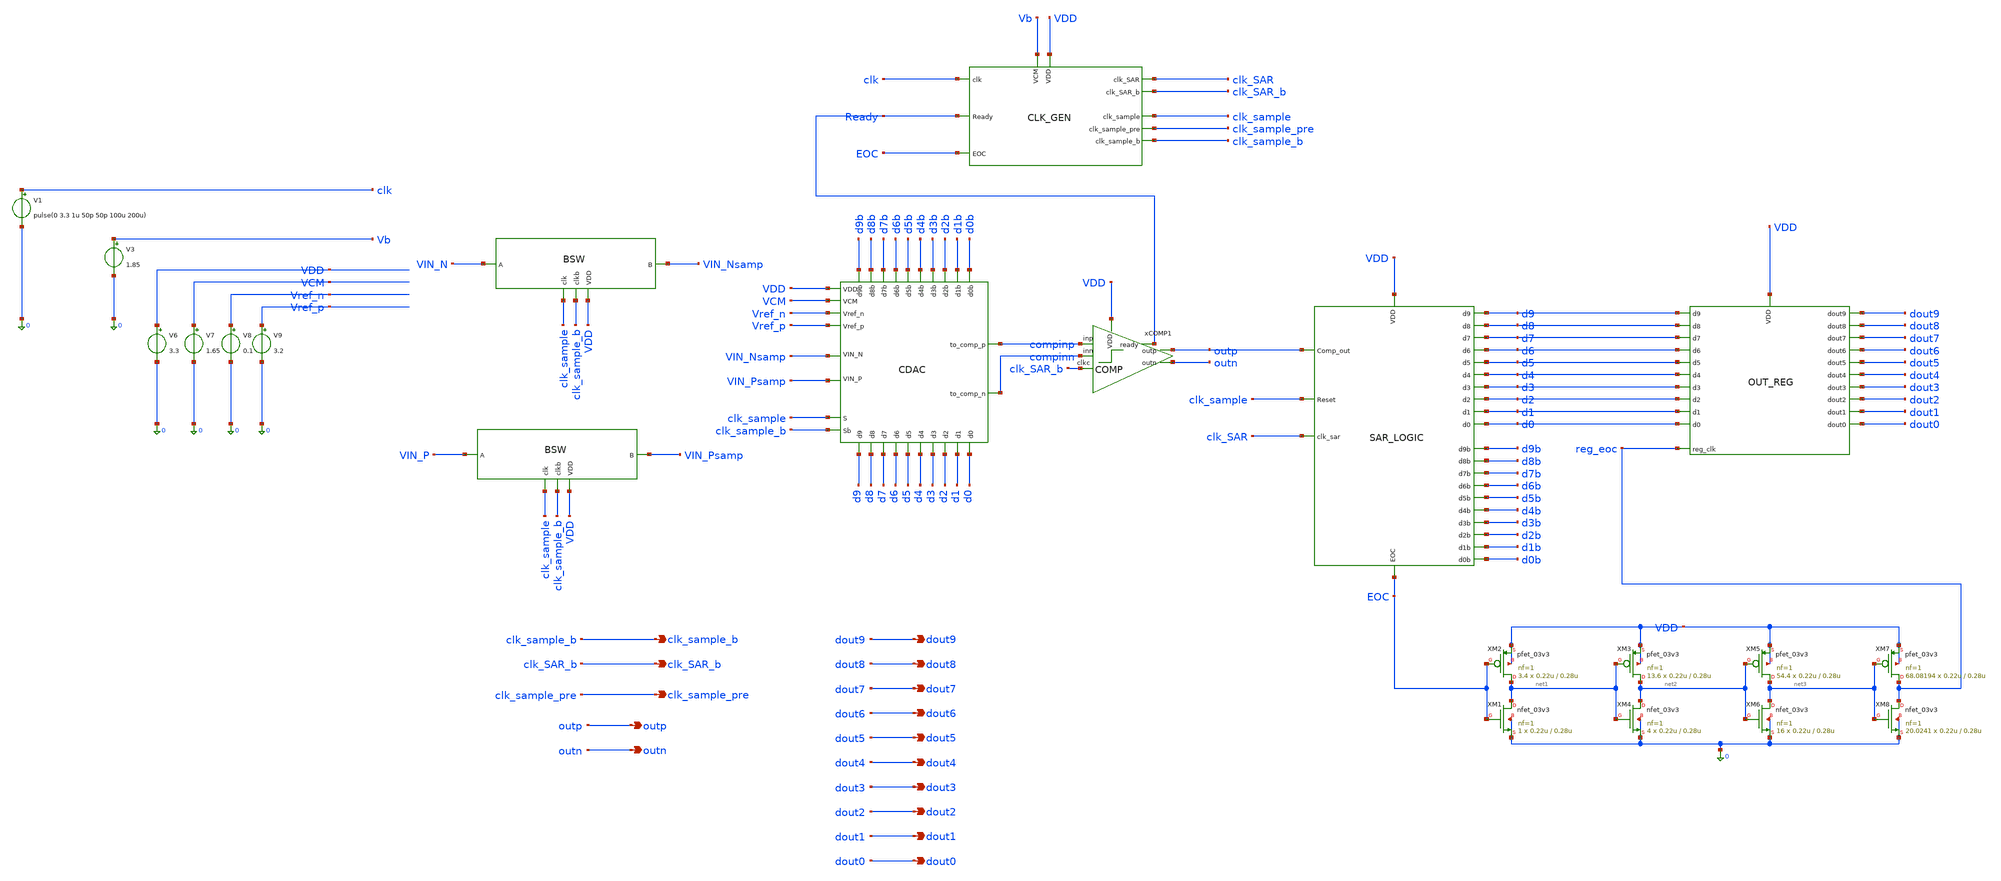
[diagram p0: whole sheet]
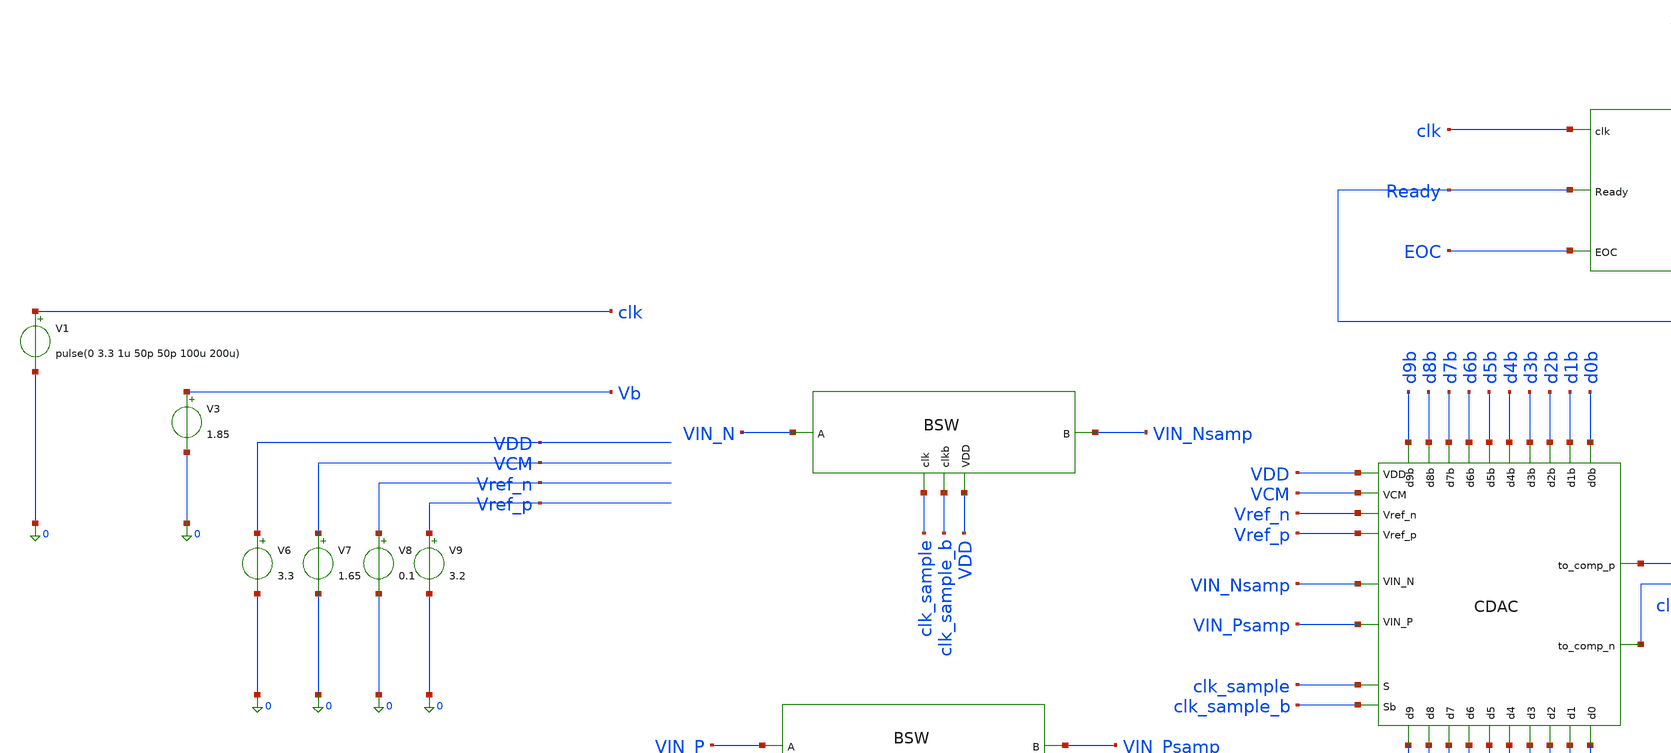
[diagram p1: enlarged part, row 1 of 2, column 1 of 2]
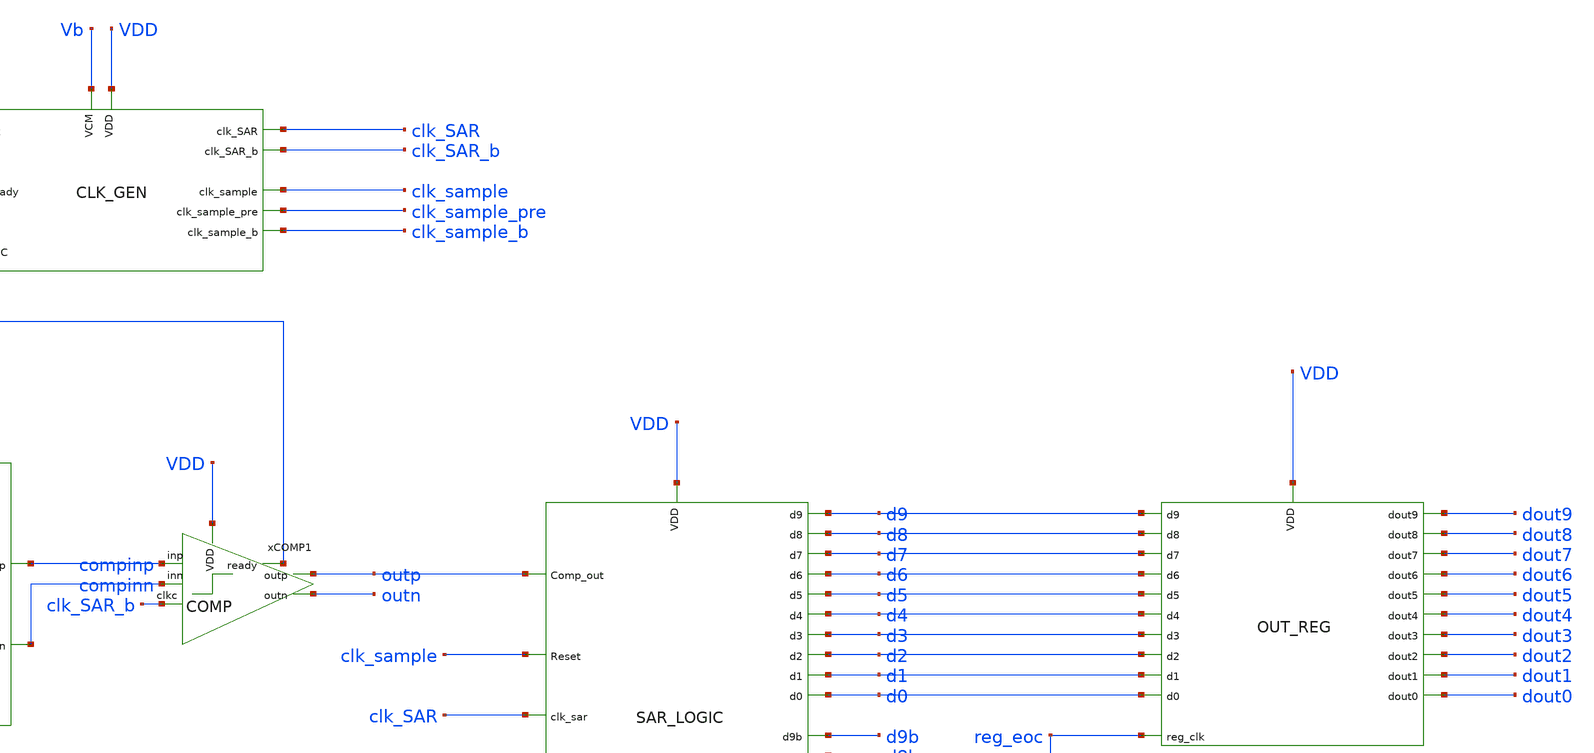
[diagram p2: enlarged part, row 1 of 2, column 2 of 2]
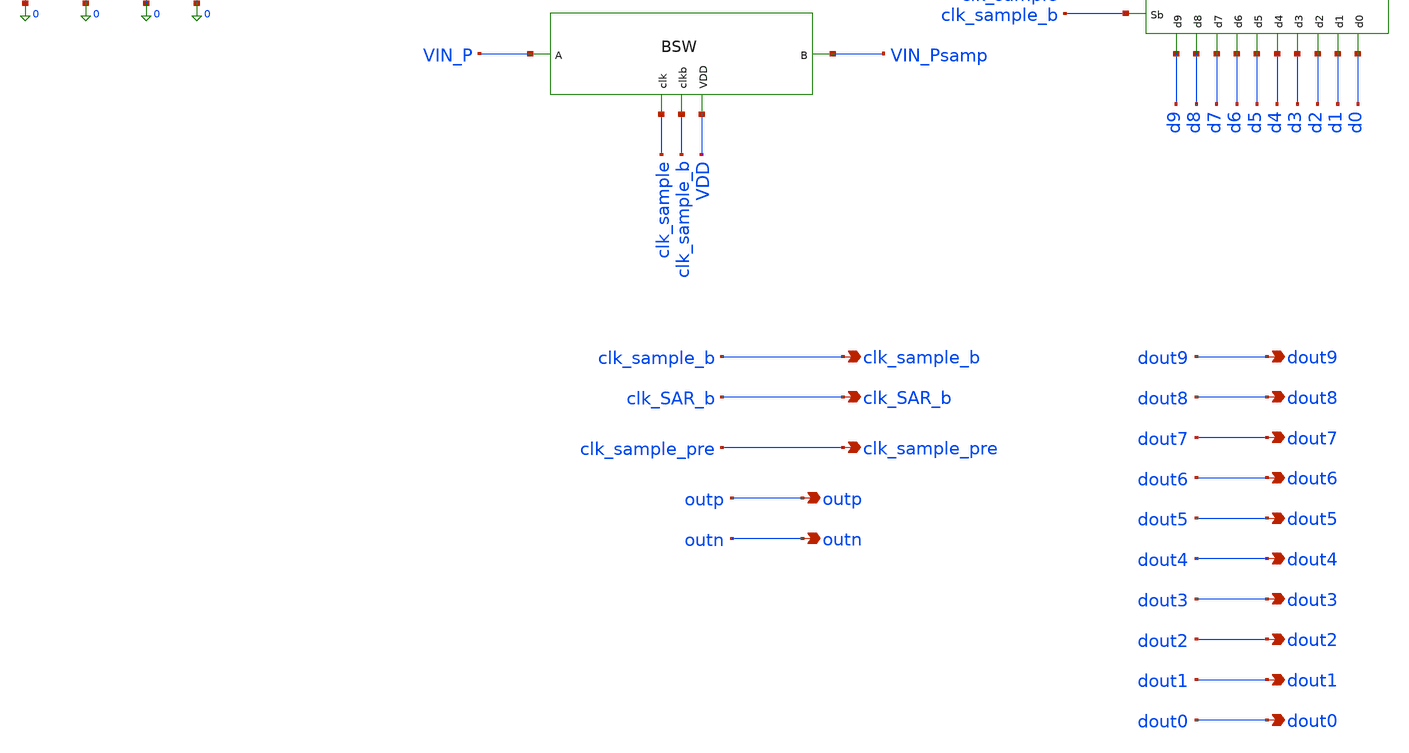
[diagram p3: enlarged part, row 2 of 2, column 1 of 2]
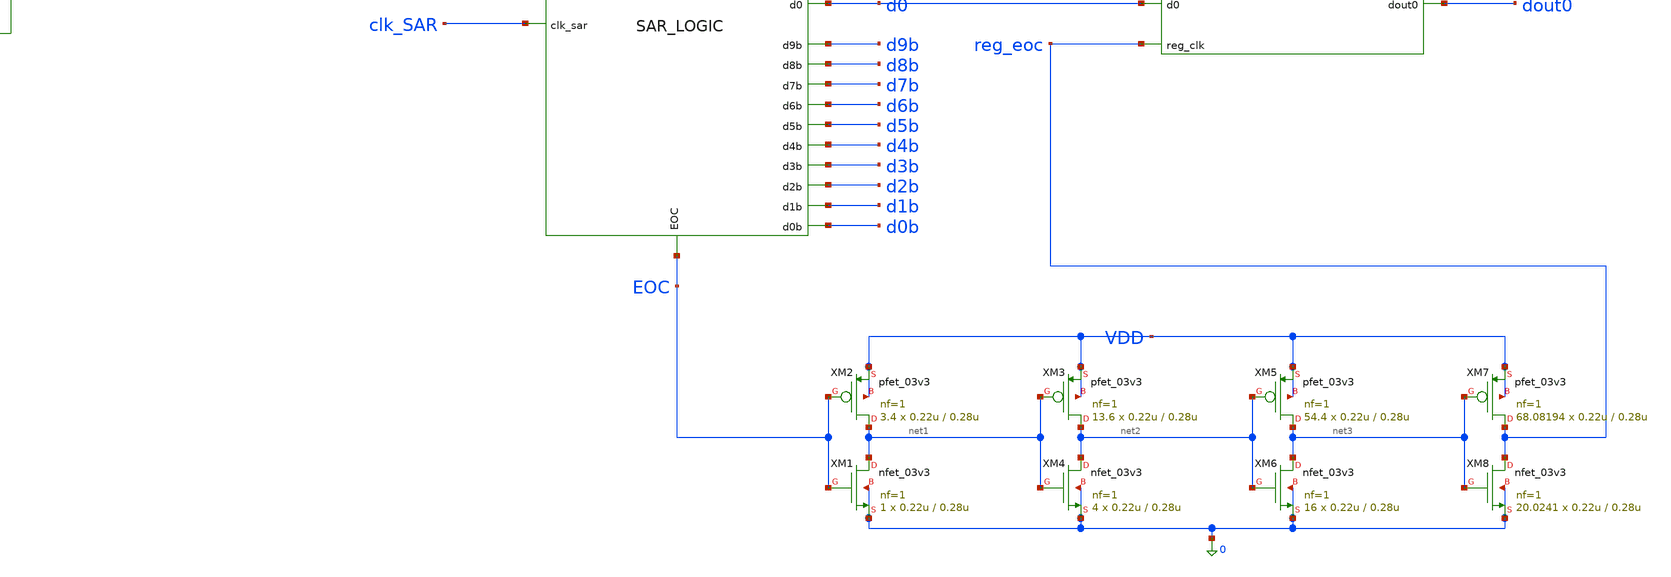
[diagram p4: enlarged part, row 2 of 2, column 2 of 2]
** sch_path: Design_Files/IC Design/Schematic/SAR_ADC_BLOCKS/SAR_ADC/SAR_ADC.sch
**.subckt SAR_ADC clk_sample_b clk_SAR_b clk_sample_pre outp outn dout9 dout8 dout7 dout6 dout5
*+ dout4 dout3 dout2 dout1 dout0
*.opin clk_sample_b
*.opin clk_SAR_b
*.opin clk_sample_pre
*.opin outp
*.opin outn
*.opin dout9
*.opin dout8
*.opin dout7
*.opin dout6
*.opin dout5
*.opin dout4
*.opin dout3
*.opin dout2
*.opin dout1
*.opin dout0
V1 clk 0 pulse(0 3.3 1u 50p 50p 100u 200u)
V3 Vb 0 1.85
V6 VDD 0 3.3
V7 VCM 0 1.65
V8 Vref_n 0 0.1
V9 Vref_p 0 3.2
XM2 net1 EOC VDD VDD pfet_03v3 L=0.28u W=0.22u nf=1 ad='int((nf+1)/2) * W/nf * 0.18u' as='int((nf+2)/2) * W/nf * 0.18u'
+ pd='2*int((nf+1)/2) * (W/nf + 0.18u)' ps='2*int((nf+2)/2) * (W/nf + 0.18u)' nrd='0.18u / W' nrs='0.18u / W'
+ sa=0 sb=0 sd=0 m=3.4
XM1 net1 EOC 0 0 nfet_03v3 L=0.28u W=0.22u nf=1 ad='int((nf+1)/2) * W/nf * 0.18u' as='int((nf+2)/2) * W/nf * 0.18u'
+ pd='2*int((nf+1)/2) * (W/nf + 0.18u)' ps='2*int((nf+2)/2) * (W/nf + 0.18u)' nrd='0.18u / W' nrs='0.18u / W'
+ sa=0 sb=0 sd=0 m=1
XM3 net2 net1 VDD VDD pfet_03v3 L=0.28u W=0.22u nf=1 ad='int((nf+1)/2) * W/nf * 0.18u' as='int((nf+2)/2) * W/nf * 0.18u'
+ pd='2*int((nf+1)/2) * (W/nf + 0.18u)' ps='2*int((nf+2)/2) * (W/nf + 0.18u)' nrd='0.18u / W' nrs='0.18u / W'
+ sa=0 sb=0 sd=0 m=13.6
XM4 net2 net1 0 0 nfet_03v3 L=0.28u W=0.22u nf=1 ad='int((nf+1)/2) * W/nf * 0.18u' as='int((nf+2)/2) * W/nf * 0.18u'
+ pd='2*int((nf+1)/2) * (W/nf + 0.18u)' ps='2*int((nf+2)/2) * (W/nf + 0.18u)' nrd='0.18u / W' nrs='0.18u / W'
+ sa=0 sb=0 sd=0 m=4
XM5 net3 net2 VDD VDD pfet_03v3 L=0.28u W=0.22u nf=1 ad='int((nf+1)/2) * W/nf * 0.18u' as='int((nf+2)/2) * W/nf * 0.18u'
+ pd='2*int((nf+1)/2) * (W/nf + 0.18u)' ps='2*int((nf+2)/2) * (W/nf + 0.18u)' nrd='0.18u / W' nrs='0.18u / W'
+ sa=0 sb=0 sd=0 m=54.4
XM6 net3 net2 0 0 nfet_03v3 L=0.28u W=0.22u nf=1 ad='int((nf+1)/2) * W/nf * 0.18u' as='int((nf+2)/2) * W/nf * 0.18u'
+ pd='2*int((nf+1)/2) * (W/nf + 0.18u)' ps='2*int((nf+2)/2) * (W/nf + 0.18u)' nrd='0.18u / W' nrs='0.18u / W'
+ sa=0 sb=0 sd=0 m=16
XM7 reg_eoc net3 VDD VDD pfet_03v3 L=0.28u W=0.22u nf=1 ad='int((nf+1)/2) * W/nf * 0.18u' as='int((nf+2)/2) * W/nf * 0.18u'
+ pd='2*int((nf+1)/2) * (W/nf + 0.18u)' ps='2*int((nf+2)/2) * (W/nf + 0.18u)' nrd='0.18u / W' nrs='0.18u / W'
+ sa=0 sb=0 sd=0 m=68.08194
XM8 reg_eoc net3 0 0 nfet_03v3 L=0.28u W=0.22u nf=1 ad='int((nf+1)/2) * W/nf * 0.18u' as='int((nf+2)/2) * W/nf * 0.18u'
+ pd='2*int((nf+1)/2) * (W/nf + 0.18u)' ps='2*int((nf+2)/2) * (W/nf + 0.18u)' nrd='0.18u / W' nrs='0.18u / W'
+ sa=0 sb=0 sd=0 m=20.0241
xBSW1 clk_sample clk_sample_b VDD VIN_N VIN_Nsamp BSW
xBSW2 clk_sample clk_sample_b VDD VIN_P VIN_Psamp BSW
xCLKGEN1 clk VDD Vb EOC Ready clk_sample_b clk_sample clk_SAR clk_SAR_b clk_sample_pre CLK_GEN
xCOMP1 VDD Ready compinp outp outn compinn clk_SAR_b COMP
xSARLOGIC1 outp clk_sample clk_SAR VDD EOC d9 d8 d7 d6 d5 d4 d3 d2 d1 d0 d9b d8b d7b d6b d5b d4b d3b
+ d2b d1b d0b SAR_LOGIC
xOUTREG1 d9 d8 d7 d6 d5 d4 d3 d2 d1 d0 VDD reg_eoc dout9 dout8 dout7 dout6 dout5 dout4 dout3 dout2
+ dout1 dout0 OUT_REG
xCDAC1 d9b d9 d8b d8 d7b d7 d6 d6b d5b d5 d4 d4b d3b d3 d2b d2 d1 d1b d0b d0 compinp VDD compinn VCM
+ clk_sample clk_sample_b VIN_Psamp VIN_Nsamp Vref_p Vref_n CDAC
**.ends
.end
